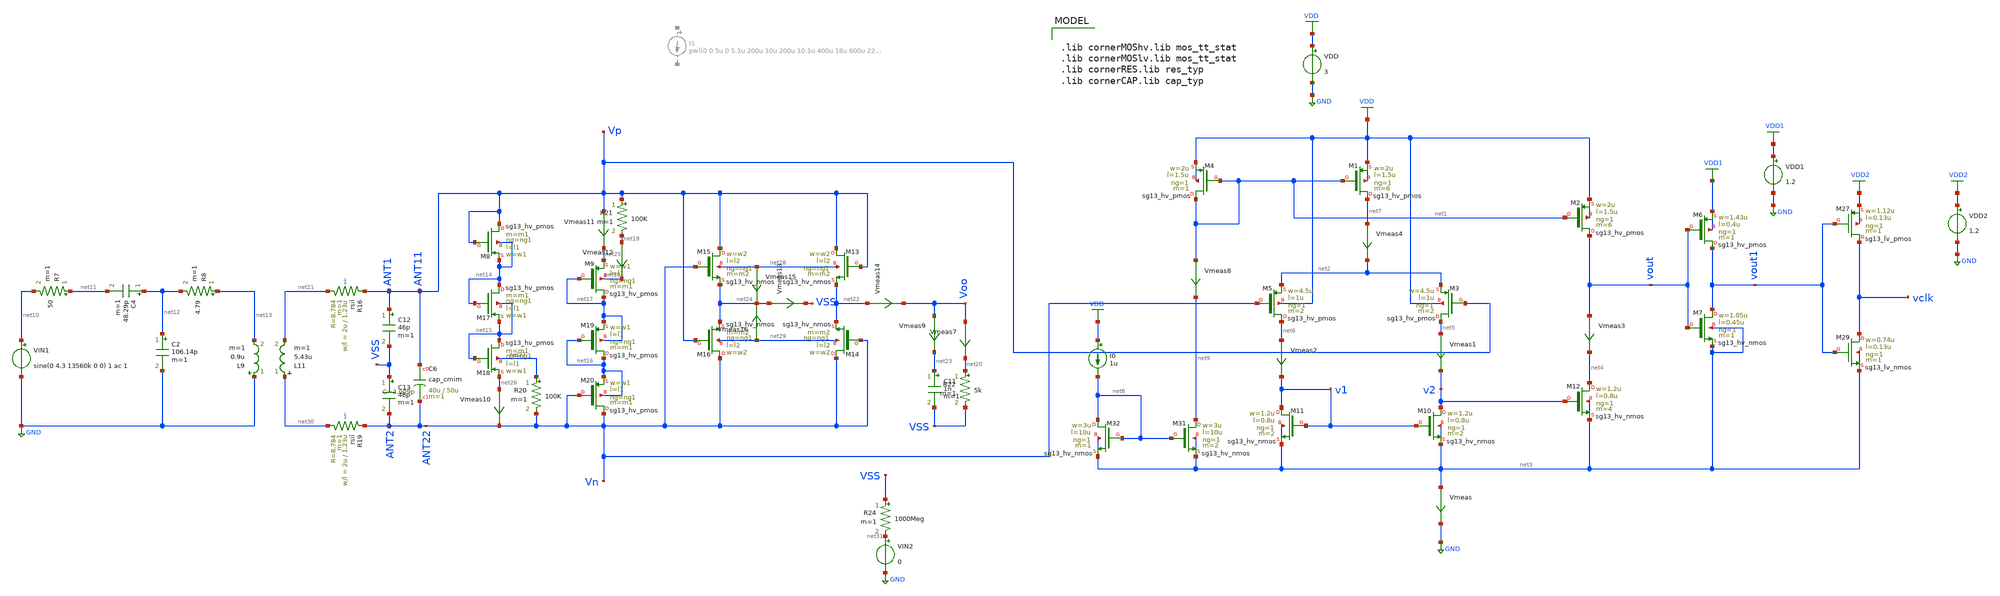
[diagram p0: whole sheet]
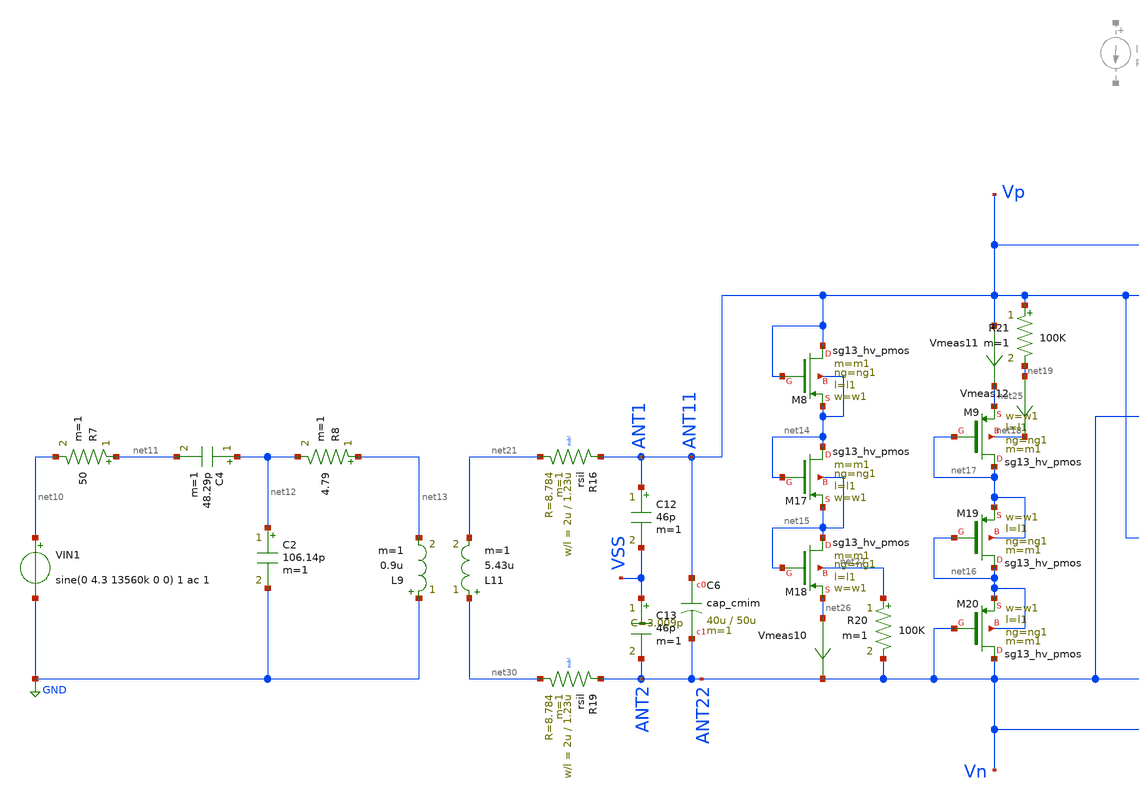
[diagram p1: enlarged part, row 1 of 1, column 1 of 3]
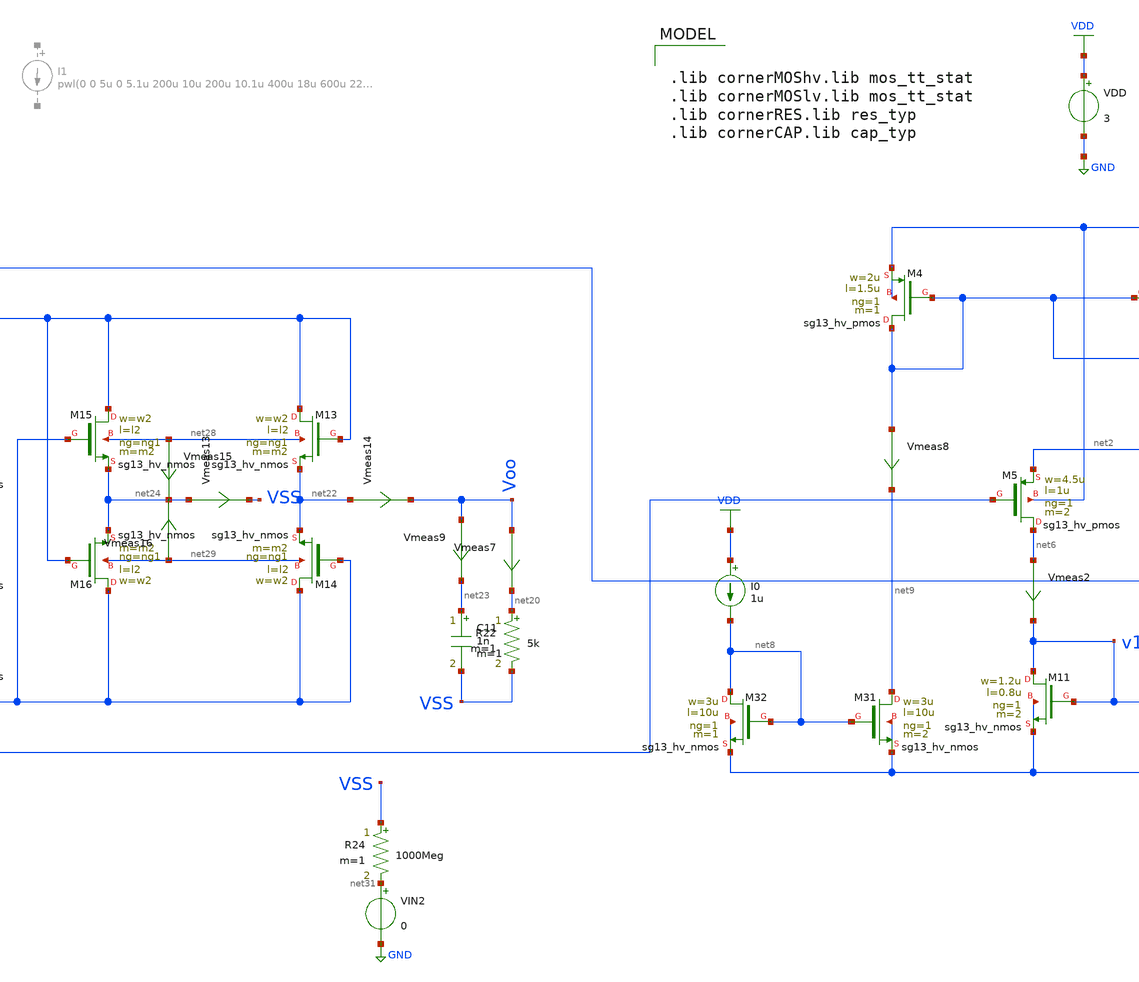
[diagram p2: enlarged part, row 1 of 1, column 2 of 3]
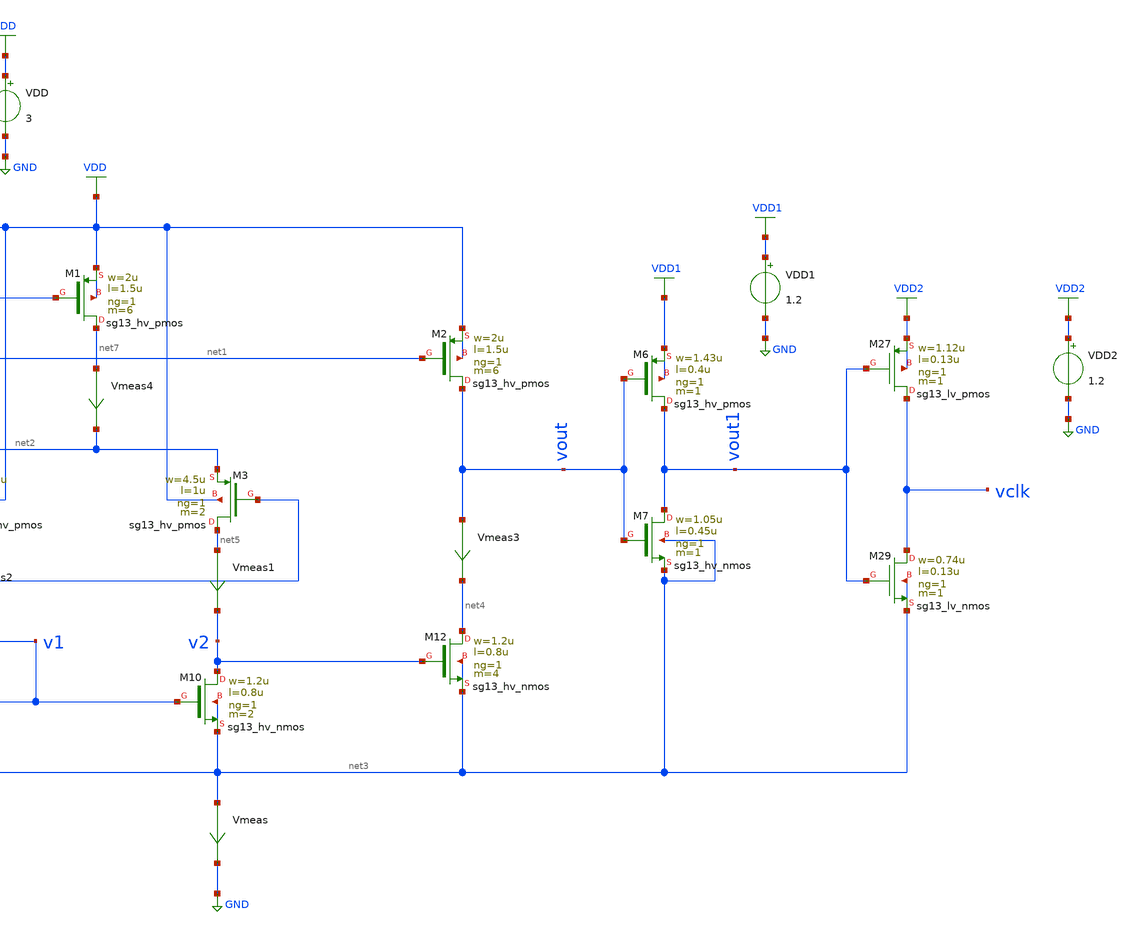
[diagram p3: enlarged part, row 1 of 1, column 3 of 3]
** sch_path: dependencies/ClockExtractor/ClockExtractor-main/schematic/xschem/schematic/MonteCarlo_Tran_10mars2026.sch
**.subckt MonteCarlo_Tran_10mars2026
VDD VDD GND 3
VDD1 VDD1 GND 1.2
XM7 vout1 vout net3 net3 sg13_hv_nmos w=1.05u l=0.45u ng=1 m=1 mm_ok=1
XM6 vout1 vout VDD1 VDD1 sg13_hv_pmos w=1.43u l=0.4u ng=1 m=1 mm_ok=1
XM4 net1 net1 VDD VDD sg13_hv_pmos w=2u l=1.5u ng=1 m=1 mm_ok=1
XM1 net7 net1 VDD VDD sg13_hv_pmos w=2u l=1.5u ng=1 m=6 mm_ok=1
XM2 vout net1 VDD VDD sg13_hv_pmos w=2u l=1.5u ng=1 m=6 mm_ok=1
XM3 net5 ANT11 net2 VDD sg13_hv_pmos w=4.5u l=1u ng=1 m=2 mm_ok=1
XM5 net6 ANT22 net2 VDD sg13_hv_pmos w=4.5u l=1u ng=1 m=2 mm_ok=1
XM10 v2 v1 net3 net3 sg13_hv_nmos w=1.2u l=0.8u ng=1 m=2 mm_ok=1
XM11 v1 v1 net3 net3 sg13_hv_nmos w=1.2u l=0.8u ng=1 m=2 mm_ok=1
XM12 net4 v2 net3 net3 sg13_hv_nmos w=1.2u l=0.8u ng=1 m=4 mm_ok=1
Vmeas net3 GND 0
.save i(vmeas)
Vmeas1 net5 v2 0
.save i(vmeas1)
Vmeas2 net6 v1 0
.save i(vmeas2)
Vmeas3 vout net4 0
.save i(vmeas3)
Vmeas4 net7 net2 0
.save i(vmeas4)
XM27 vclk vout1 VDD2 VDD2 sg13_lv_pmos w=1.12u l=0.13u ng=1 m=1 mm_ok=1
XM29 vclk vout1 net3 net3 sg13_lv_nmos w=0.74u l=0.13u ng=1 m=1 mm_ok=1
VDD2 VDD2 GND 1.2
XM31 net9 net8 net3 net3 sg13_hv_nmos w=3u l=10u ng=1 m=2 mm_ok=1
XM32 net8 net8 net3 net3 sg13_hv_nmos w=3u l=10u ng=1 m=1 mm_ok=1
Vmeas8 net1 net9 0
.save i(vmeas8)
I0 VDD net8 1u
VIN1 net10 GND sine(0 4.3 13560k 0 0) 1 ac 1

L9 GND net13 0.9u m=1
C2 net12 GND 106.14p m=1
R7 net11 net10 50 m=1
C4 net12 net11 48.29p m=1
R8 net13 net12 4.79 m=1
L11 net30 net21 5.43u m=1
XR16 ANT11 net21 sub! rsil w=2u l=1.23u m=1 mm_ok=1
XR19 ANT22 net30 sub! rsil w=2u l=1.23u m=1 mm_ok=1
XC6 ANT11 ANT22 cap_cmim w=40u l=50u m=1 mm_ok=1
XM8 ANT11 ANT11 net14 net14 sg13_hv_pmos w=w1 l=l1 ng=ng1 m=m1 mm_ok=1
XM9 net17 net17 net25 net18 sg13_hv_pmos w=w1 l=l1 ng=ng1 m=m1 mm_ok=1
R20 net27 ANT22 100K m=1
R21 ANT11 net19 100K m=1
XM13 ANT11 ANT11 net22 net28 sg13_hv_nmos w=w2 l=l2 ng=ng1 m=m2 mm_ok=1
XM14 ANT22 ANT22 net22 net29 sg13_hv_nmos w=w2 l=l2 ng=ng1 m=m2 mm_ok=1
C11 net23 VSS 1n m=1
R22 net20 VSS 5k m=1
Vmeas12 net19 net18 0
.save i(vmeas12)
C12 ANT11 VSS 46p m=1
C13 VSS ANT22 46p m=1
XM15 ANT11 ANT22 net24 net28 sg13_hv_nmos w=w2 l=l2 ng=ng1 m=m2 mm_ok=1
XM16 ANT22 ANT11 net24 net29 sg13_hv_nmos w=w2 l=l2 ng=ng1 m=m2 mm_ok=1
XM17 net14 net14 net15 net15 sg13_hv_pmos w=w1 l=l1 ng=ng1 m=m1 mm_ok=1
XM18 net15 net15 net26 net27 sg13_hv_pmos w=w1 l=l1 ng=ng1 m=m1 mm_ok=1
XM19 net16 net16 net17 net17 sg13_hv_pmos w=w1 l=l1 ng=ng1 m=m1 mm_ok=1
XM20 ANT22 ANT22 net16 net16 sg13_hv_pmos w=w1 l=l1 ng=ng1 m=m1 mm_ok=1
Vmeas7 Voo net20 0
.save i(vmeas7)
Vmeas9 Voo net23 0
.save i(vmeas9)
Vmeas10 net26 ANT22 0
.save i(vmeas10)
Vmeas11 ANT11 net25 0
.save i(vmeas11)
Vmeas13 net24 VSS 0
.save i(vmeas13)
Vmeas14 net22 Voo 0
.save i(vmeas14)
Vmeas15 net28 net24 0
.save i(vmeas15)
Vmeas16 net29 net24 0
.save i(vmeas16)
R24 VSS net31 1000Meg m=1
VIN2 net31 GND 0
**** begin user architecture code

.lib cornerMOShv.lib mos_tt_stat
.lib cornerMOSlv.lib mos_tt_stat
.lib cornerRES.lib res_typ
.lib cornerCAP.lib cap_typ




K1 L9 L11  0.7

.param mm_ok=1
.param mc_ok=1
.param temp  = 27
.param w1=5u
.param w2=10u
.param l1=0.5u
.param l2=1u
.param ng1=1
.param m1=20
.param m2=10
.param Coef=0.1
.save all
.control

let mc_runs = 200
let run = 0

shell rm MonteCarlo_Tran_10mars2026.csv

set curplot=new
set scratch=$curplot
setplot $scratch

dowhile run < mc_runs

tran 50p 2.2u

  meas tran t1 when v(vclk)=0.6 rise=19
  meas tran t2 when v(vclk)=0.6 rise=20
  let period = (t2 - t1)
  let freq = 1/period

print freq >> MonteCarlo_Tran_10mars2026.csv

set run=$&run
set ac=$curplot
setplot $scratch

let out{$run}={$ac}.vclk
let temp{$run}={$ac}.time
setplot $ac
reset
let run=run+1
end

//plot {$scratch}.all vs {$scratch}.temp0
//wrdata MonteCarlo_Tran_2026.csv  {$scratch}.freq
//echo 'Monte Carlo Simulation Completed.'
//echo 'Frequencies saved in MonteCarlo_Freq.csv'

write MonteCarlo_Tran_2026.raw
.endc


**** end user architecture code
**.ends
.GLOBAL GND
.GLOBAL VDD
.GLOBAL VDD1
.GLOBAL VDD2
.end
